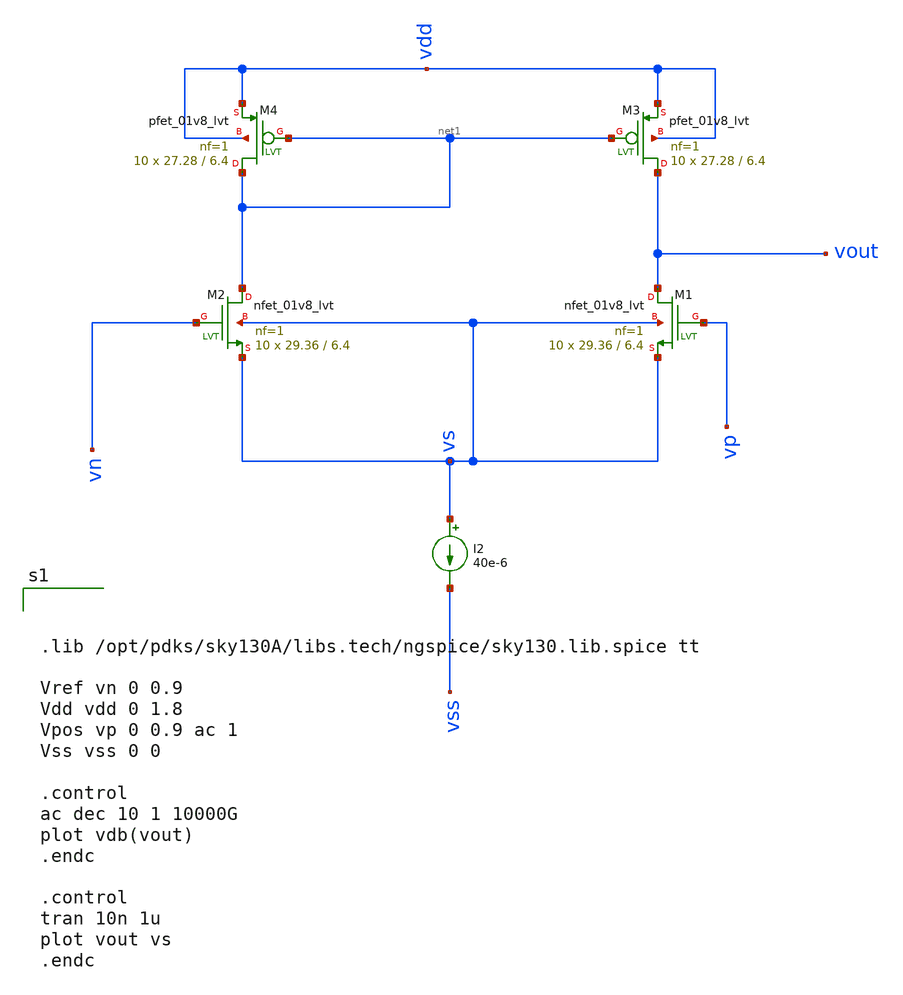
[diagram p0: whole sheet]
** sch_path: test/sstadex/untitled.sch
**.subckt untitled
I2 vs vss 40e-6
XM1 vout vp vs vs sky130_fd_pr__nfet_01v8_lvt L=6.4 W=29.36 nf=1 ad='int((nf+1)/2) * W/nf * 0.29' as='int((nf+2)/2) * W/nf * 0.29'
+ pd='2*int((nf+1)/2) * (W/nf + 0.29)' ps='2*int((nf+2)/2) * (W/nf + 0.29)' nrd='0.29 / W' nrs='0.29 / W'
+ sa=0 sb=0 sd=0 mult=10 m=10
XM2 net1 vn vs vs sky130_fd_pr__nfet_01v8_lvt L=6.4 W=29.36 nf=1 ad='int((nf+1)/2) * W/nf * 0.29' as='int((nf+2)/2) * W/nf * 0.29'
+ pd='2*int((nf+1)/2) * (W/nf + 0.29)' ps='2*int((nf+2)/2) * (W/nf + 0.29)' nrd='0.29 / W' nrs='0.29 / W'
+ sa=0 sb=0 sd=0 mult=10 m=10
XM3 vout net1 vdd vdd sky130_fd_pr__pfet_01v8_lvt L=6.4 W=27.28 nf=1 ad='int((nf+1)/2) * W/nf * 0.29'
+ as='int((nf+2)/2) * W/nf * 0.29' pd='2*int((nf+1)/2) * (W/nf + 0.29)' ps='2*int((nf+2)/2) * (W/nf + 0.29)'
+ nrd='0.29 / W' nrs='0.29 / W' sa=0 sb=0 sd=0 mult=10 m=10
XM4 net1 net1 vdd vdd sky130_fd_pr__pfet_01v8_lvt L=6.4 W=27.28 nf=1 ad='int((nf+1)/2) * W/nf * 0.29'
+ as='int((nf+2)/2) * W/nf * 0.29' pd='2*int((nf+1)/2) * (W/nf + 0.29)' ps='2*int((nf+2)/2) * (W/nf + 0.29)'
+ nrd='0.29 / W' nrs='0.29 / W' sa=0 sb=0 sd=0 mult=10 m=10
**** begin user architecture code



.lib /opt/pdks/sky130A/libs.tech/ngspice/sky130.lib.spice tt

Vref vn 0 0.9
Vdd vdd 0 1.8
Vpos vp 0 0.9 ac 1
Vss vss 0 0

.control
ac dec 10 1 10000G
plot vdb(vout)
.endc

.control
tran 10n 1u
plot vout vs
.endc



**** end user architecture code
**.ends
.end
